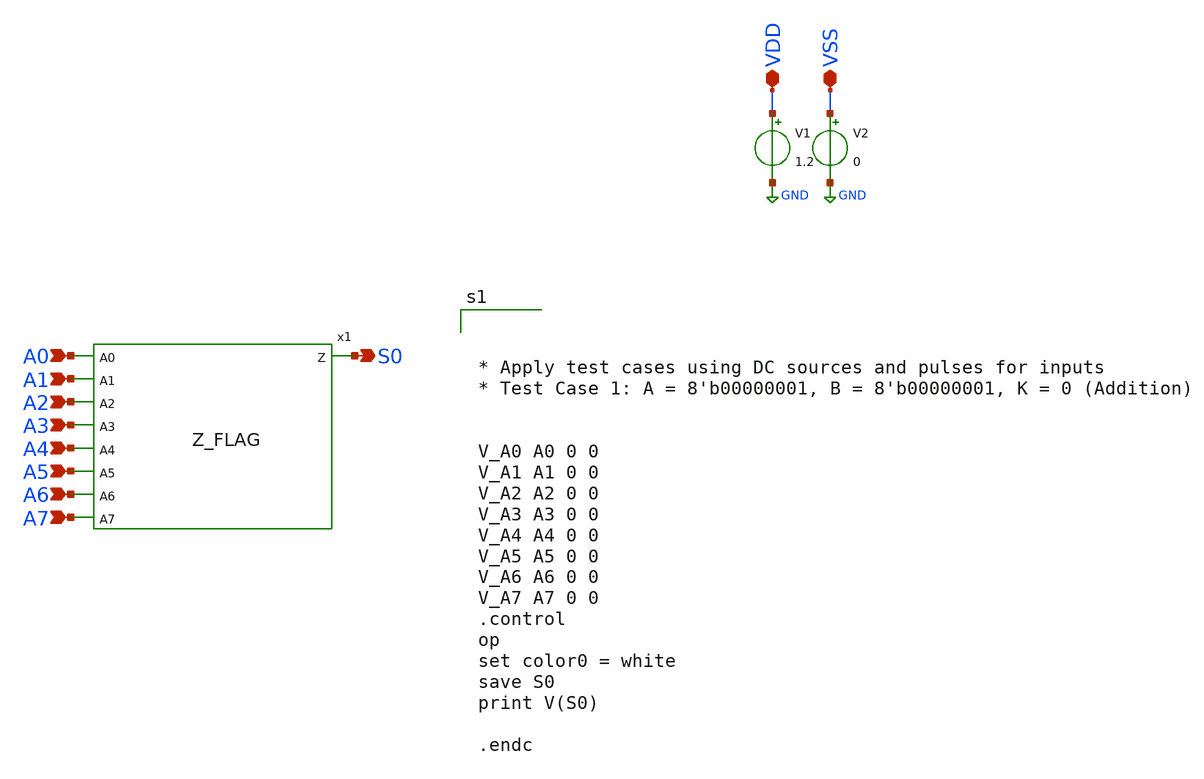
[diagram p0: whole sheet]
** sch_path: design/xschem/TEST_BENCHES/Z_FLAG_TB.sch
**.subckt Z_FLAG_TB A0 A1 A2 A3 A4 A5 A6 A7 S0 VDD VSS
*.ipin A0
*.ipin A1
*.ipin A2
*.ipin A3
*.ipin A4
*.ipin A5
*.ipin A6
*.ipin A7
*.opin S0
*.iopin VDD
*.iopin VSS
V1 VDD GND 1.2
V2 VSS GND 0
x1 A0 A1 A2 A3 S0 A4 A5 A6 A7 VSS VDD Z_FLAG
**** begin user architecture code

** opencircuitdesign pdks install
.lib $::SKYWATER_MODELS/sky130.lib.spice tt_mm





* Apply test cases using DC sources and pulses for inputs
* Test Case 1: A = 8'b00000001, B = 8'b00000001, K = 0 (Addition)


V_A0 A0 0 0
V_A1 A1 0 0
V_A2 A2 0 0
V_A3 A3 0 0
V_A4 A4 0 0
V_A5 A5 0 0
V_A6 A6 0 0
V_A7 A7 0 0
.control
op
set color0 = white
save S0
print V(S0)

.endc


**** end user architecture code
**.ends

* expanding   symbol:  ZV_FLAG/Z_FLAG.sym # of pins=9
** sym_path: design/xschem/ZV_FLAG/Z_FLAG.sym
** sch_path: design/xschem/ZV_FLAG/Z_FLAG.sch
.subckt Z_FLAG A0 A1 A2 A3 Z A4 A5 A6 A7 VSS VDD
*.ipin A0
*.ipin A1
*.ipin A2
*.ipin A3
*.ipin A4
*.ipin A5
*.ipin A6
*.ipin A7
*.opin Z
x2 A0 A1 A2 A3 VSS VDD net2 nor4
x3 A4 A5 A6 A7 VSS VDD net1 nor4
x1 net2 net1 VSS VDD Z and2
.ends


* expanding   symbol:  NOR/nor4.sym # of pins=5
** sym_path: design/xschem/NOR/nor4.sym
** sch_path: design/xschem/NOR/nor4.sch
.subckt nor4 A B C D VSS VDD Y
*.ipin A
*.opin Y
*.ipin B
*.ipin C
*.ipin D
XM1 Y A net1 net1 sky130_fd_pr__pfet_01v8 L=0.15 W=12.8 nf=1 ad='int((nf+1)/2) * W/nf * 0.29' as='int((nf+2)/2) * W/nf * 0.29'
+ pd='2*int((nf+1)/2) * (W/nf + 0.29)' ps='2*int((nf+2)/2) * (W/nf + 0.29)' nrd='0.29 / W' nrs='0.29 / W'
+ sa=0 sb=0 sd=0 mult=1 m=1
XM2 Y A VSS VSS sky130_fd_pr__nfet_01v8 L=0.15 W=1 nf=1 ad='int((nf+1)/2) * W/nf * 0.29' as='int((nf+2)/2) * W/nf * 0.29'
+ pd='2*int((nf+1)/2) * (W/nf + 0.29)' ps='2*int((nf+2)/2) * (W/nf + 0.29)' nrd='0.29 / W' nrs='0.29 / W'
+ sa=0 sb=0 sd=0 mult=1 m=1
XM3 Y B VSS VSS sky130_fd_pr__nfet_01v8 L=0.15 W=1 nf=1 ad='int((nf+1)/2) * W/nf * 0.29' as='int((nf+2)/2) * W/nf * 0.29'
+ pd='2*int((nf+1)/2) * (W/nf + 0.29)' ps='2*int((nf+2)/2) * (W/nf + 0.29)' nrd='0.29 / W' nrs='0.29 / W'
+ sa=0 sb=0 sd=0 mult=1 m=1
XM4 net1 B net3 net3 sky130_fd_pr__pfet_01v8 L=0.15 W=12.8 nf=1 ad='int((nf+1)/2) * W/nf * 0.29' as='int((nf+2)/2) * W/nf * 0.29'
+ pd='2*int((nf+1)/2) * (W/nf + 0.29)' ps='2*int((nf+2)/2) * (W/nf + 0.29)' nrd='0.29 / W' nrs='0.29 / W'
+ sa=0 sb=0 sd=0 mult=1 m=1
XM5 net3 C net2 net2 sky130_fd_pr__pfet_01v8 L=0.15 W=12.8 nf=1 ad='int((nf+1)/2) * W/nf * 0.29' as='int((nf+2)/2) * W/nf * 0.29'
+ pd='2*int((nf+1)/2) * (W/nf + 0.29)' ps='2*int((nf+2)/2) * (W/nf + 0.29)' nrd='0.29 / W' nrs='0.29 / W'
+ sa=0 sb=0 sd=0 mult=1 m=1
XM6 Y C VSS VSS sky130_fd_pr__nfet_01v8 L=0.15 W=1 nf=1 ad='int((nf+1)/2) * W/nf * 0.29' as='int((nf+2)/2) * W/nf * 0.29'
+ pd='2*int((nf+1)/2) * (W/nf + 0.29)' ps='2*int((nf+2)/2) * (W/nf + 0.29)' nrd='0.29 / W' nrs='0.29 / W'
+ sa=0 sb=0 sd=0 mult=1 m=1
XM7 Y D VSS VSS sky130_fd_pr__nfet_01v8 L=0.15 W=1 nf=1 ad='int((nf+1)/2) * W/nf * 0.29' as='int((nf+2)/2) * W/nf * 0.29'
+ pd='2*int((nf+1)/2) * (W/nf + 0.29)' ps='2*int((nf+2)/2) * (W/nf + 0.29)' nrd='0.29 / W' nrs='0.29 / W'
+ sa=0 sb=0 sd=0 mult=1 m=1
XM8 net2 D VDD VDD sky130_fd_pr__pfet_01v8 L=0.15 W=12.8 nf=1 ad='int((nf+1)/2) * W/nf * 0.29' as='int((nf+2)/2) * W/nf * 0.29'
+ pd='2*int((nf+1)/2) * (W/nf + 0.29)' ps='2*int((nf+2)/2) * (W/nf + 0.29)' nrd='0.29 / W' nrs='0.29 / W'
+ sa=0 sb=0 sd=0 mult=1 m=1
.ends


* expanding   symbol:  AND/and2.sym # of pins=3
** sym_path: design/xschem/AND/and2.sym
** sch_path: design/xschem/AND/and2.sch
.subckt and2 A B VSS VDD Y
*.ipin A
*.ipin B
*.opin Y
x1 net1 VSS VDD Y inv
x2 A B VSS VDD net1 nand2
.ends


* expanding   symbol:  INV/inv.sym # of pins=2
** sym_path: design/xschem/INV/inv.sym
** sch_path: design/xschem/INV/inv.sch
.subckt inv A VSS VDD Y
*.ipin A
*.opin Y
XM2 Y A VSS GND sky130_fd_pr__nfet_01v8 L=0.15 W=1 nf=1 ad='int((nf+1)/2) * W/nf * 0.29' as='int((nf+2)/2) * W/nf * 0.29'
+ pd='2*int((nf+1)/2) * (W/nf + 0.29)' ps='2*int((nf+2)/2) * (W/nf + 0.29)' nrd='0.29 / W' nrs='0.29 / W'
+ sa=0 sb=0 sd=0 mult=1 m=1
XM1 Y A VDD VDD sky130_fd_pr__pfet_01v8 L=0.15 W=3.21 nf=1 ad='int((nf+1)/2) * W/nf * 0.29' as='int((nf+2)/2) * W/nf * 0.29'
+ pd='2*int((nf+1)/2) * (W/nf + 0.29)' ps='2*int((nf+2)/2) * (W/nf + 0.29)' nrd='0.29 / W' nrs='0.29 / W'
+ sa=0 sb=0 sd=0 mult=1 m=1
.ends


* expanding   symbol:  NAND/nand2.sym # of pins=3
** sym_path: design/xschem/NAND/nand2.sym
** sch_path: design/xschem/NAND/nand2.sch
.subckt nand2 A B VSS VDD Y
*.ipin A
*.opin Y
*.ipin B
XM1 Y A VDD VDD sky130_fd_pr__pfet_01v8 L=0.15 W=3.2 nf=1 ad='int((nf+1)/2) * W/nf * 0.29' as='int((nf+2)/2) * W/nf * 0.29'
+ pd='2*int((nf+1)/2) * (W/nf + 0.29)' ps='2*int((nf+2)/2) * (W/nf + 0.29)' nrd='0.29 / W' nrs='0.29 / W'
+ sa=0 sb=0 sd=0 mult=1 m=1
XM2 Y A net1 net1 sky130_fd_pr__nfet_01v8 L=0.15 W=2 nf=1 ad='int((nf+1)/2) * W/nf * 0.29' as='int((nf+2)/2) * W/nf * 0.29'
+ pd='2*int((nf+1)/2) * (W/nf + 0.29)' ps='2*int((nf+2)/2) * (W/nf + 0.29)' nrd='0.29 / W' nrs='0.29 / W'
+ sa=0 sb=0 sd=0 mult=1 m=1
XM3 net1 B VSS VSS sky130_fd_pr__nfet_01v8 L=0.15 W=2 nf=1 ad='int((nf+1)/2) * W/nf * 0.29' as='int((nf+2)/2) * W/nf * 0.29'
+ pd='2*int((nf+1)/2) * (W/nf + 0.29)' ps='2*int((nf+2)/2) * (W/nf + 0.29)' nrd='0.29 / W' nrs='0.29 / W'
+ sa=0 sb=0 sd=0 mult=1 m=1
XM4 Y B VDD VDD sky130_fd_pr__pfet_01v8 L=0.15 W=3.2 nf=1 ad='int((nf+1)/2) * W/nf * 0.29' as='int((nf+2)/2) * W/nf * 0.29'
+ pd='2*int((nf+1)/2) * (W/nf + 0.29)' ps='2*int((nf+2)/2) * (W/nf + 0.29)' nrd='0.29 / W' nrs='0.29 / W'
+ sa=0 sb=0 sd=0 mult=1 m=1
.ends

.GLOBAL GND
.end
